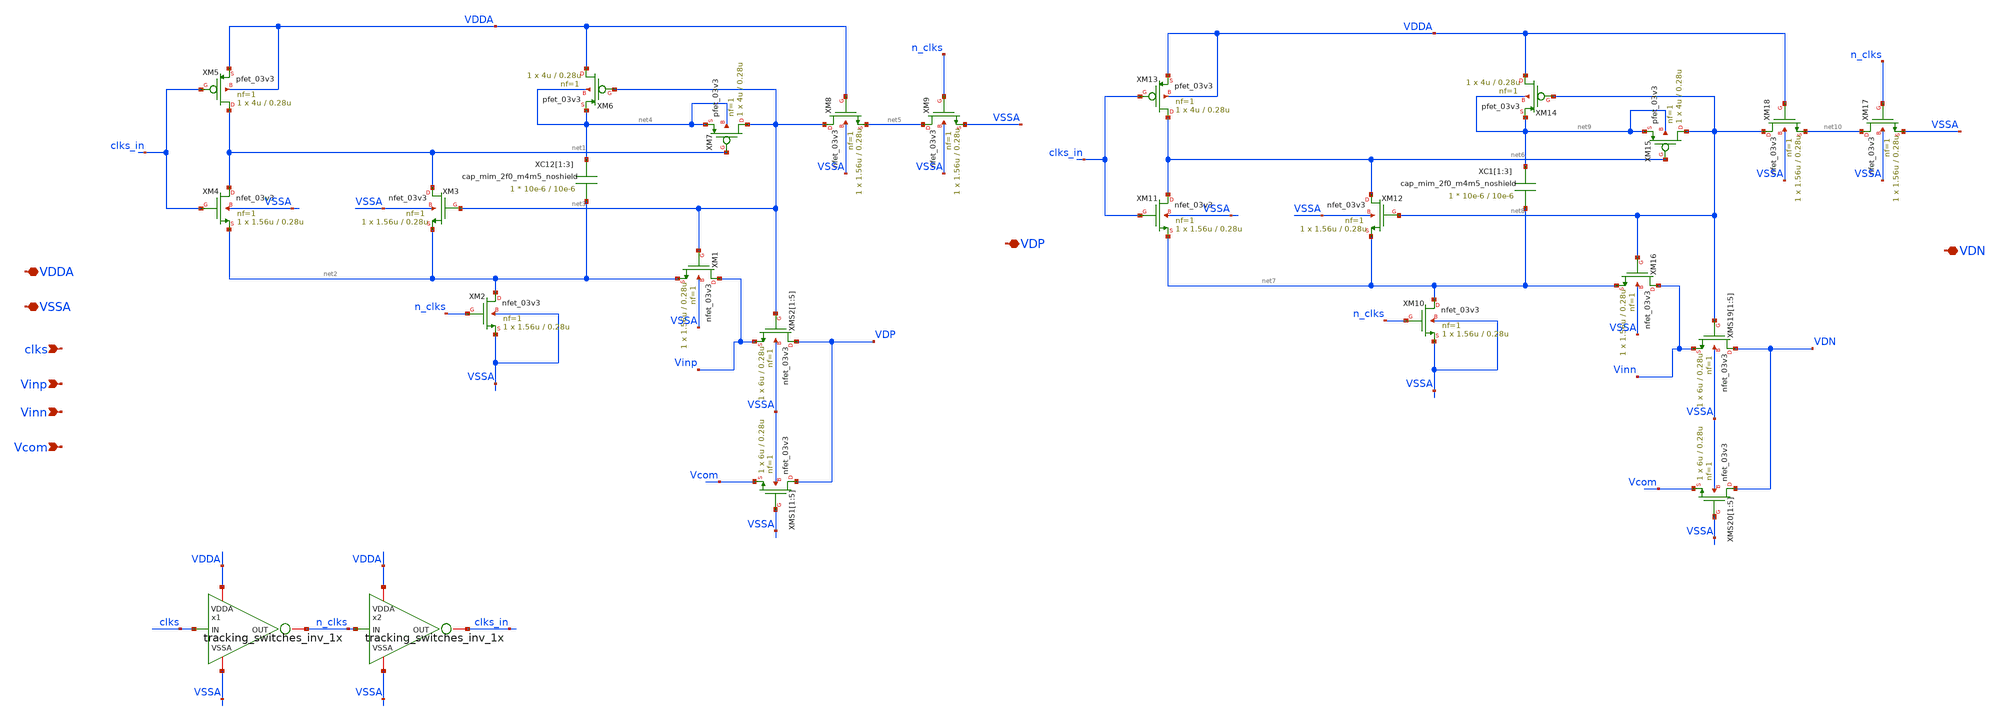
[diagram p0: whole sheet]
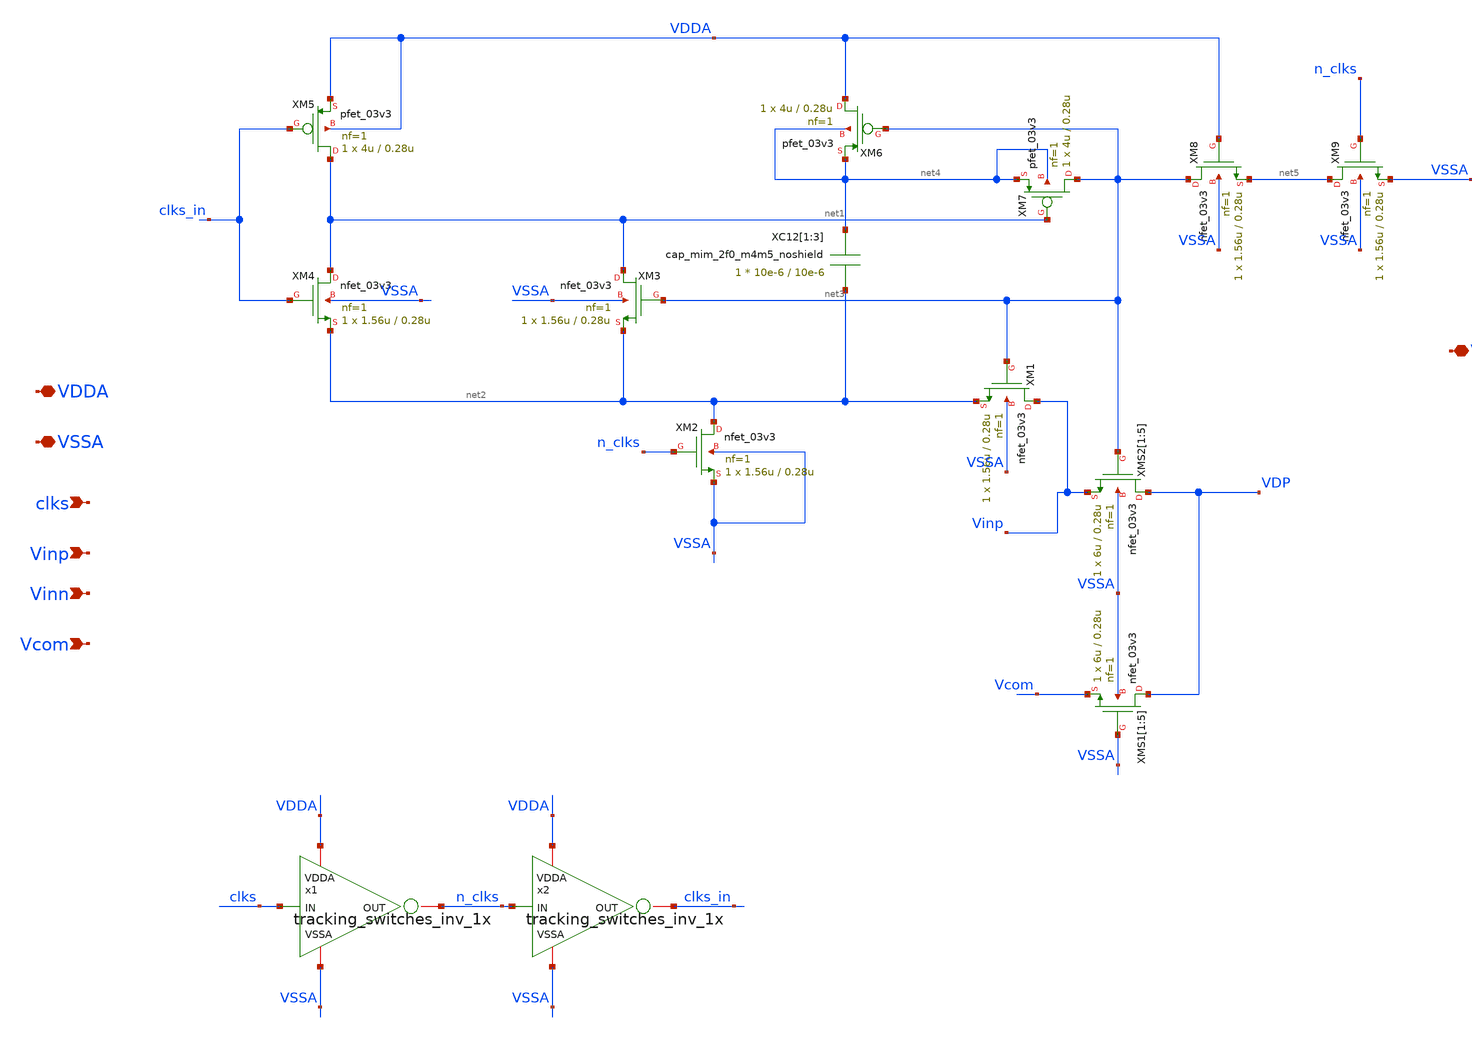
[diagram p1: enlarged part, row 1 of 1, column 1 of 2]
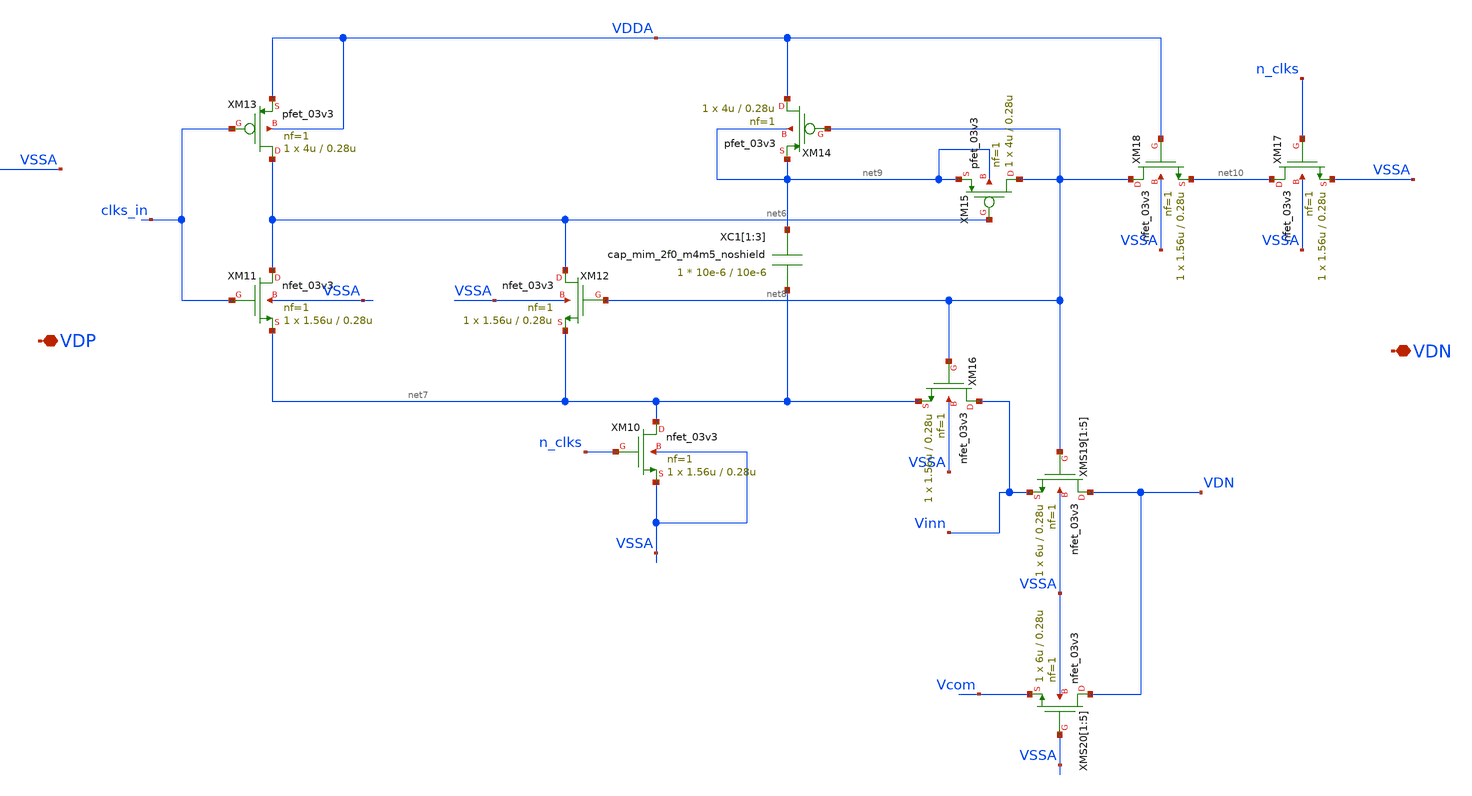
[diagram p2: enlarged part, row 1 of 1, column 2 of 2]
** sch_path: SAR_ADC/tracking_switches/xschem/tracking_switches.sch
**.subckt tracking_switches VDDA VSSA clks Vinp VDP Vinn VDN Vcom
*.iopin VDDA
*.iopin VSSA
*.ipin clks
*.ipin Vinp
*.iopin VDP
*.ipin Vinn
*.iopin VDN
*.ipin Vcom
XM2 net2 n_clks VSSA VSSA nfet_03v3 L=0.28u W=1.56u nf=1 ad='int((nf+1)/2) * W/nf * 0.18u' as='int((nf+2)/2) * W/nf * 0.18u'
+ pd='2*int((nf+1)/2) * (W/nf + 0.18u)' ps='2*int((nf+2)/2) * (W/nf + 0.18u)' nrd='0.18u / W' nrs='0.18u / W'
+ sa=0 sb=0 sd=0 m=1
XM4 net1 clks_in net2 VSSA nfet_03v3 L=0.28u W=1.56u nf=1 ad='int((nf+1)/2) * W/nf * 0.18u' as='int((nf+2)/2) * W/nf * 0.18u'
+ pd='2*int((nf+1)/2) * (W/nf + 0.18u)' ps='2*int((nf+2)/2) * (W/nf + 0.18u)' nrd='0.18u / W' nrs='0.18u / W'
+ sa=0 sb=0 sd=0 m=1
XM3 net1 net3 net2 VSSA nfet_03v3 L=0.28u W=1.56u nf=1 ad='int((nf+1)/2) * W/nf * 0.18u' as='int((nf+2)/2) * W/nf * 0.18u'
+ pd='2*int((nf+1)/2) * (W/nf + 0.18u)' ps='2*int((nf+2)/2) * (W/nf + 0.18u)' nrd='0.18u / W' nrs='0.18u / W'
+ sa=0 sb=0 sd=0 m=1
XM5 net1 clks_in VDDA VDDA pfet_03v3 L=0.28u W=4u nf=1 ad='int((nf+1)/2) * W/nf * 0.18u' as='int((nf+2)/2) * W/nf * 0.18u'
+ pd='2*int((nf+1)/2) * (W/nf + 0.18u)' ps='2*int((nf+2)/2) * (W/nf + 0.18u)' nrd='0.18u / W' nrs='0.18u / W'
+ sa=0 sb=0 sd=0 m=1
XM6 VDDA net3 net4 net4 pfet_03v3 L=0.28u W=4u nf=1 ad='int((nf+1)/2) * W/nf * 0.18u' as='int((nf+2)/2) * W/nf * 0.18u'
+ pd='2*int((nf+1)/2) * (W/nf + 0.18u)' ps='2*int((nf+2)/2) * (W/nf + 0.18u)' nrd='0.18u / W' nrs='0.18u / W'
+ sa=0 sb=0 sd=0 m=1
XM7 net3 net1 net4 net4 pfet_03v3 L=0.28u W=4u nf=1 ad='int((nf+1)/2) * W/nf * 0.18u' as='int((nf+2)/2) * W/nf * 0.18u'
+ pd='2*int((nf+1)/2) * (W/nf + 0.18u)' ps='2*int((nf+2)/2) * (W/nf + 0.18u)' nrd='0.18u / W' nrs='0.18u / W'
+ sa=0 sb=0 sd=0 m=1
XM1 Vinp net3 net2 VSSA nfet_03v3 L=0.28u W=1.56u nf=1 ad='int((nf+1)/2) * W/nf * 0.18u' as='int((nf+2)/2) * W/nf * 0.18u'
+ pd='2*int((nf+1)/2) * (W/nf + 0.18u)' ps='2*int((nf+2)/2) * (W/nf + 0.18u)' nrd='0.18u / W' nrs='0.18u / W'
+ sa=0 sb=0 sd=0 m=1
XM9 net5 n_clks VSSA VSSA nfet_03v3 L=0.28u W=1.56u nf=1 ad='int((nf+1)/2) * W/nf * 0.18u' as='int((nf+2)/2) * W/nf * 0.18u'
+ pd='2*int((nf+1)/2) * (W/nf + 0.18u)' ps='2*int((nf+2)/2) * (W/nf + 0.18u)' nrd='0.18u / W' nrs='0.18u / W'
+ sa=0 sb=0 sd=0 m=1
XM8 net3 VDDA net5 VSSA nfet_03v3 L=0.28u W=1.56u nf=1 ad='int((nf+1)/2) * W/nf * 0.18u' as='int((nf+2)/2) * W/nf * 0.18u'
+ pd='2*int((nf+1)/2) * (W/nf + 0.18u)' ps='2*int((nf+2)/2) * (W/nf + 0.18u)' nrd='0.18u / W' nrs='0.18u / W'
+ sa=0 sb=0 sd=0 m=1
x1 VDDA VSSA n_clks clks tracking_switches_inv_1x
x2 VDDA VSSA clks_in n_clks tracking_switches_inv_1x
XMS2[1] VDP net3 Vinp VSSA nfet_03v3 L=0.28u W=6u nf=1 ad='int((nf+1)/2) * W/nf * 0.18u' as='int((nf+2)/2) * W/nf * 0.18u'
+ pd='2*int((nf+1)/2) * (W/nf + 0.18u)' ps='2*int((nf+2)/2) * (W/nf + 0.18u)' nrd='0.18u / W' nrs='0.18u / W'
+ sa=0 sb=0 sd=0 m=1
XMS2[2] VDP net3 Vinp VSSA nfet_03v3 L=0.28u W=6u nf=1 ad='int((nf+1)/2) * W/nf * 0.18u' as='int((nf+2)/2) * W/nf * 0.18u'
+ pd='2*int((nf+1)/2) * (W/nf + 0.18u)' ps='2*int((nf+2)/2) * (W/nf + 0.18u)' nrd='0.18u / W' nrs='0.18u / W'
+ sa=0 sb=0 sd=0 m=1
XMS2[3] VDP net3 Vinp VSSA nfet_03v3 L=0.28u W=6u nf=1 ad='int((nf+1)/2) * W/nf * 0.18u' as='int((nf+2)/2) * W/nf * 0.18u'
+ pd='2*int((nf+1)/2) * (W/nf + 0.18u)' ps='2*int((nf+2)/2) * (W/nf + 0.18u)' nrd='0.18u / W' nrs='0.18u / W'
+ sa=0 sb=0 sd=0 m=1
XMS2[4] VDP net3 Vinp VSSA nfet_03v3 L=0.28u W=6u nf=1 ad='int((nf+1)/2) * W/nf * 0.18u' as='int((nf+2)/2) * W/nf * 0.18u'
+ pd='2*int((nf+1)/2) * (W/nf + 0.18u)' ps='2*int((nf+2)/2) * (W/nf + 0.18u)' nrd='0.18u / W' nrs='0.18u / W'
+ sa=0 sb=0 sd=0 m=1
XMS2[5] VDP net3 Vinp VSSA nfet_03v3 L=0.28u W=6u nf=1 ad='int((nf+1)/2) * W/nf * 0.18u' as='int((nf+2)/2) * W/nf * 0.18u'
+ pd='2*int((nf+1)/2) * (W/nf + 0.18u)' ps='2*int((nf+2)/2) * (W/nf + 0.18u)' nrd='0.18u / W' nrs='0.18u / W'
+ sa=0 sb=0 sd=0 m=1
XC12[1] net4 net2 cap_mim_2f0_m4m5_noshield c_width=10e-6 c_length=10e-6 m=1
XC12[2] net4 net2 cap_mim_2f0_m4m5_noshield c_width=10e-6 c_length=10e-6 m=1
XC12[3] net4 net2 cap_mim_2f0_m4m5_noshield c_width=10e-6 c_length=10e-6 m=1
XMS1[1] VDP VSSA Vcom VSSA nfet_03v3 L=0.28u W=6u nf=1 ad='int((nf+1)/2) * W/nf * 0.18u' as='int((nf+2)/2) * W/nf * 0.18u'
+ pd='2*int((nf+1)/2) * (W/nf + 0.18u)' ps='2*int((nf+2)/2) * (W/nf + 0.18u)' nrd='0.18u / W' nrs='0.18u / W'
+ sa=0 sb=0 sd=0 m=1
XMS1[2] VDP VSSA Vcom VSSA nfet_03v3 L=0.28u W=6u nf=1 ad='int((nf+1)/2) * W/nf * 0.18u' as='int((nf+2)/2) * W/nf * 0.18u'
+ pd='2*int((nf+1)/2) * (W/nf + 0.18u)' ps='2*int((nf+2)/2) * (W/nf + 0.18u)' nrd='0.18u / W' nrs='0.18u / W'
+ sa=0 sb=0 sd=0 m=1
XMS1[3] VDP VSSA Vcom VSSA nfet_03v3 L=0.28u W=6u nf=1 ad='int((nf+1)/2) * W/nf * 0.18u' as='int((nf+2)/2) * W/nf * 0.18u'
+ pd='2*int((nf+1)/2) * (W/nf + 0.18u)' ps='2*int((nf+2)/2) * (W/nf + 0.18u)' nrd='0.18u / W' nrs='0.18u / W'
+ sa=0 sb=0 sd=0 m=1
XMS1[4] VDP VSSA Vcom VSSA nfet_03v3 L=0.28u W=6u nf=1 ad='int((nf+1)/2) * W/nf * 0.18u' as='int((nf+2)/2) * W/nf * 0.18u'
+ pd='2*int((nf+1)/2) * (W/nf + 0.18u)' ps='2*int((nf+2)/2) * (W/nf + 0.18u)' nrd='0.18u / W' nrs='0.18u / W'
+ sa=0 sb=0 sd=0 m=1
XMS1[5] VDP VSSA Vcom VSSA nfet_03v3 L=0.28u W=6u nf=1 ad='int((nf+1)/2) * W/nf * 0.18u' as='int((nf+2)/2) * W/nf * 0.18u'
+ pd='2*int((nf+1)/2) * (W/nf + 0.18u)' ps='2*int((nf+2)/2) * (W/nf + 0.18u)' nrd='0.18u / W' nrs='0.18u / W'
+ sa=0 sb=0 sd=0 m=1
XM10 net7 n_clks VSSA VSSA nfet_03v3 L=0.28u W=1.56u nf=1 ad='int((nf+1)/2) * W/nf * 0.18u' as='int((nf+2)/2) * W/nf * 0.18u'
+ pd='2*int((nf+1)/2) * (W/nf + 0.18u)' ps='2*int((nf+2)/2) * (W/nf + 0.18u)' nrd='0.18u / W' nrs='0.18u / W'
+ sa=0 sb=0 sd=0 m=1
XM11 net6 clks_in net7 VSSA nfet_03v3 L=0.28u W=1.56u nf=1 ad='int((nf+1)/2) * W/nf * 0.18u' as='int((nf+2)/2) * W/nf * 0.18u'
+ pd='2*int((nf+1)/2) * (W/nf + 0.18u)' ps='2*int((nf+2)/2) * (W/nf + 0.18u)' nrd='0.18u / W' nrs='0.18u / W'
+ sa=0 sb=0 sd=0 m=1
XM12 net6 net8 net7 VSSA nfet_03v3 L=0.28u W=1.56u nf=1 ad='int((nf+1)/2) * W/nf * 0.18u' as='int((nf+2)/2) * W/nf * 0.18u'
+ pd='2*int((nf+1)/2) * (W/nf + 0.18u)' ps='2*int((nf+2)/2) * (W/nf + 0.18u)' nrd='0.18u / W' nrs='0.18u / W'
+ sa=0 sb=0 sd=0 m=1
XM13 net6 clks_in VDDA VDDA pfet_03v3 L=0.28u W=4u nf=1 ad='int((nf+1)/2) * W/nf * 0.18u' as='int((nf+2)/2) * W/nf * 0.18u'
+ pd='2*int((nf+1)/2) * (W/nf + 0.18u)' ps='2*int((nf+2)/2) * (W/nf + 0.18u)' nrd='0.18u / W' nrs='0.18u / W'
+ sa=0 sb=0 sd=0 m=1
XM14 VDDA net8 net9 net9 pfet_03v3 L=0.28u W=4u nf=1 ad='int((nf+1)/2) * W/nf * 0.18u' as='int((nf+2)/2) * W/nf * 0.18u'
+ pd='2*int((nf+1)/2) * (W/nf + 0.18u)' ps='2*int((nf+2)/2) * (W/nf + 0.18u)' nrd='0.18u / W' nrs='0.18u / W'
+ sa=0 sb=0 sd=0 m=1
XM15 net8 net6 net9 net9 pfet_03v3 L=0.28u W=4u nf=1 ad='int((nf+1)/2) * W/nf * 0.18u' as='int((nf+2)/2) * W/nf * 0.18u'
+ pd='2*int((nf+1)/2) * (W/nf + 0.18u)' ps='2*int((nf+2)/2) * (W/nf + 0.18u)' nrd='0.18u / W' nrs='0.18u / W'
+ sa=0 sb=0 sd=0 m=1
XM16 Vinn net8 net7 VSSA nfet_03v3 L=0.28u W=1.56u nf=1 ad='int((nf+1)/2) * W/nf * 0.18u' as='int((nf+2)/2) * W/nf * 0.18u'
+ pd='2*int((nf+1)/2) * (W/nf + 0.18u)' ps='2*int((nf+2)/2) * (W/nf + 0.18u)' nrd='0.18u / W' nrs='0.18u / W'
+ sa=0 sb=0 sd=0 m=1
XM17 net10 n_clks VSSA VSSA nfet_03v3 L=0.28u W=1.56u nf=1 ad='int((nf+1)/2) * W/nf * 0.18u' as='int((nf+2)/2) * W/nf * 0.18u'
+ pd='2*int((nf+1)/2) * (W/nf + 0.18u)' ps='2*int((nf+2)/2) * (W/nf + 0.18u)' nrd='0.18u / W' nrs='0.18u / W'
+ sa=0 sb=0 sd=0 m=1
XM18 net8 VDDA net10 VSSA nfet_03v3 L=0.28u W=1.56u nf=1 ad='int((nf+1)/2) * W/nf * 0.18u' as='int((nf+2)/2) * W/nf * 0.18u'
+ pd='2*int((nf+1)/2) * (W/nf + 0.18u)' ps='2*int((nf+2)/2) * (W/nf + 0.18u)' nrd='0.18u / W' nrs='0.18u / W'
+ sa=0 sb=0 sd=0 m=1
XMS19[1] VDN net8 Vinn VSSA nfet_03v3 L=0.28u W=6u nf=1 ad='int((nf+1)/2) * W/nf * 0.18u' as='int((nf+2)/2) * W/nf * 0.18u'
+ pd='2*int((nf+1)/2) * (W/nf + 0.18u)' ps='2*int((nf+2)/2) * (W/nf + 0.18u)' nrd='0.18u / W' nrs='0.18u / W'
+ sa=0 sb=0 sd=0 m=1
XMS19[2] VDN net8 Vinn VSSA nfet_03v3 L=0.28u W=6u nf=1 ad='int((nf+1)/2) * W/nf * 0.18u' as='int((nf+2)/2) * W/nf * 0.18u'
+ pd='2*int((nf+1)/2) * (W/nf + 0.18u)' ps='2*int((nf+2)/2) * (W/nf + 0.18u)' nrd='0.18u / W' nrs='0.18u / W'
+ sa=0 sb=0 sd=0 m=1
XMS19[3] VDN net8 Vinn VSSA nfet_03v3 L=0.28u W=6u nf=1 ad='int((nf+1)/2) * W/nf * 0.18u' as='int((nf+2)/2) * W/nf * 0.18u'
+ pd='2*int((nf+1)/2) * (W/nf + 0.18u)' ps='2*int((nf+2)/2) * (W/nf + 0.18u)' nrd='0.18u / W' nrs='0.18u / W'
+ sa=0 sb=0 sd=0 m=1
XMS19[4] VDN net8 Vinn VSSA nfet_03v3 L=0.28u W=6u nf=1 ad='int((nf+1)/2) * W/nf * 0.18u' as='int((nf+2)/2) * W/nf * 0.18u'
+ pd='2*int((nf+1)/2) * (W/nf + 0.18u)' ps='2*int((nf+2)/2) * (W/nf + 0.18u)' nrd='0.18u / W' nrs='0.18u / W'
+ sa=0 sb=0 sd=0 m=1
XMS19[5] VDN net8 Vinn VSSA nfet_03v3 L=0.28u W=6u nf=1 ad='int((nf+1)/2) * W/nf * 0.18u' as='int((nf+2)/2) * W/nf * 0.18u'
+ pd='2*int((nf+1)/2) * (W/nf + 0.18u)' ps='2*int((nf+2)/2) * (W/nf + 0.18u)' nrd='0.18u / W' nrs='0.18u / W'
+ sa=0 sb=0 sd=0 m=1
XC1[1] net9 net7 cap_mim_2f0_m4m5_noshield c_width=10e-6 c_length=10e-6 m=1
XC1[2] net9 net7 cap_mim_2f0_m4m5_noshield c_width=10e-6 c_length=10e-6 m=1
XC1[3] net9 net7 cap_mim_2f0_m4m5_noshield c_width=10e-6 c_length=10e-6 m=1
XMS20[1] VDN VSSA Vcom VSSA nfet_03v3 L=0.28u W=6u nf=1 ad='int((nf+1)/2) * W/nf * 0.18u' as='int((nf+2)/2) * W/nf * 0.18u'
+ pd='2*int((nf+1)/2) * (W/nf + 0.18u)' ps='2*int((nf+2)/2) * (W/nf + 0.18u)' nrd='0.18u / W' nrs='0.18u / W'
+ sa=0 sb=0 sd=0 m=1
XMS20[2] VDN VSSA Vcom VSSA nfet_03v3 L=0.28u W=6u nf=1 ad='int((nf+1)/2) * W/nf * 0.18u' as='int((nf+2)/2) * W/nf * 0.18u'
+ pd='2*int((nf+1)/2) * (W/nf + 0.18u)' ps='2*int((nf+2)/2) * (W/nf + 0.18u)' nrd='0.18u / W' nrs='0.18u / W'
+ sa=0 sb=0 sd=0 m=1
XMS20[3] VDN VSSA Vcom VSSA nfet_03v3 L=0.28u W=6u nf=1 ad='int((nf+1)/2) * W/nf * 0.18u' as='int((nf+2)/2) * W/nf * 0.18u'
+ pd='2*int((nf+1)/2) * (W/nf + 0.18u)' ps='2*int((nf+2)/2) * (W/nf + 0.18u)' nrd='0.18u / W' nrs='0.18u / W'
+ sa=0 sb=0 sd=0 m=1
XMS20[4] VDN VSSA Vcom VSSA nfet_03v3 L=0.28u W=6u nf=1 ad='int((nf+1)/2) * W/nf * 0.18u' as='int((nf+2)/2) * W/nf * 0.18u'
+ pd='2*int((nf+1)/2) * (W/nf + 0.18u)' ps='2*int((nf+2)/2) * (W/nf + 0.18u)' nrd='0.18u / W' nrs='0.18u / W'
+ sa=0 sb=0 sd=0 m=1
XMS20[5] VDN VSSA Vcom VSSA nfet_03v3 L=0.28u W=6u nf=1 ad='int((nf+1)/2) * W/nf * 0.18u' as='int((nf+2)/2) * W/nf * 0.18u'
+ pd='2*int((nf+1)/2) * (W/nf + 0.18u)' ps='2*int((nf+2)/2) * (W/nf + 0.18u)' nrd='0.18u / W' nrs='0.18u / W'
+ sa=0 sb=0 sd=0 m=1
**.ends

* expanding   symbol:  PICO_contest/tracking_switches/xschem/tracking_switches_inv_1x.sym # of
*+ pins=4
** sym_path: SAR_ADC/blocks/tracking_switches/tracking_switches_inv_1x.sym
** sch_path: SAR_ADC/blocks/tracking_switches/tracking_switches_inv_1x.sch
.subckt tracking_switches_inv_1x VDDA VSSA OUT IN
*.iopin VDDA
*.iopin VSSA
*.iopin OUT
*.ipin IN
XM1 OUT IN VSSA VSSA nfet_03v3 L=0.28u W=0.22u nf=1 ad='int((nf+1)/2) * W/nf * 0.18u' as='int((nf+2)/2) * W/nf * 0.18u'
+ pd='2*int((nf+1)/2) * (W/nf + 0.18u)' ps='2*int((nf+2)/2) * (W/nf + 0.18u)' nrd='0.18u / W' nrs='0.18u / W'
+ sa=0 sb=0 sd=0 m=1
XM2 OUT IN VDDA VDDA pfet_03v3 L=0.28u W=0.66u nf=1 ad='int((nf+1)/2) * W/nf * 0.18u' as='int((nf+2)/2) * W/nf * 0.18u'
+ pd='2*int((nf+1)/2) * (W/nf + 0.18u)' ps='2*int((nf+2)/2) * (W/nf + 0.18u)' nrd='0.18u / W' nrs='0.18u / W'
+ sa=0 sb=0 sd=0 m=1
.ends

.end
